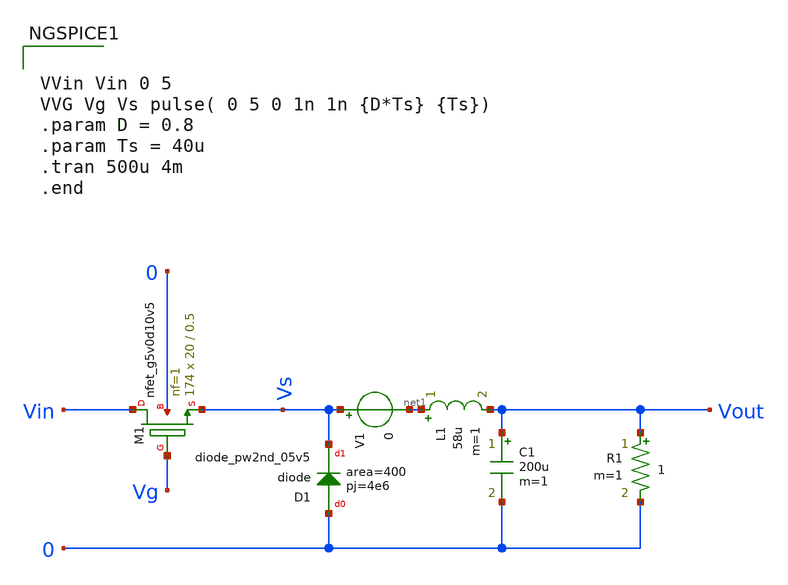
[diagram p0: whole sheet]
** sch_path: Analog_blocks/Analog_Blocks/DC_DC converter/Testbench/Buck_converter.sch
**.subckt Buck_converter
C1 Vout 0 200u m=1
L1 net1 Vout 58u m=1
R1 Vout 0 1 m=1
XM1 Vin Vg Vs 0 sky130_fd_pr__nfet_g5v0d10v5 L=0.5 W=20 nf=1 ad='int((nf+1)/2) * W/nf * 0.29' as='int((nf+2)/2) * W/nf * 0.29'
+ pd='2*int((nf+1)/2) * (W/nf + 0.29)' ps='2*int((nf+2)/2) * (W/nf + 0.29)' nrd='0.29 / W' nrs='0.29 / W'
+ sa=0 sb=0 sd=0 mult=174 m=174
V1 Vs net1 0
XD1 0 Vs sky130_fd_pr__diode_pw2nd_05v5 area=400 pj=4e6
**** begin user architecture code


VVin Vin 0 5
VVG Vg Vs pulse( 0 5 0 1n 1n {D*Ts} {Ts})
.param D = 0.8
.param Ts = 40u
.tran 500u 4m
.end




.param mc_mm_switch=0
.param mc_pr_switch=0
.include ~/mabrains/Analog_blocks/models/sky130A/libs.ref/sky130_fd_pr/spice/sky130_fd_pr__nfet_01v8__tt.corner.spice
.include ~/mabrains/Analog_blocks/models/sky130A/libs.ref/sky130_fd_pr/spice/sky130_fd_pr__nfet_01v8_lvt__tt.corner.spice
.include ~/mabrains/Analog_blocks/models/sky130A/libs.ref/sky130_fd_pr/spice/sky130_fd_pr__pfet_01v8__tt.corner.spice
.include ~/mabrains/Analog_blocks/models/sky130A/libs.ref/sky130_fd_pr/spice/sky130_fd_pr__nfet_03v3_nvt__tt.corner.spice
.include ~/mabrains/Analog_blocks/models/sky130A/libs.ref/sky130_fd_pr/spice/sky130_fd_pr__nfet_05v0_nvt__tt.corner.spice
.include ~/mabrains/Analog_blocks/models/sky130A/libs.ref/sky130_fd_pr/spice/sky130_fd_pr__esd_nfet_01v8__tt.corner.spice
.include ~/mabrains/Analog_blocks/models/sky130A/libs.ref/sky130_fd_pr/spice/sky130_fd_pr__pfet_01v8_lvt__tt.corner.spice
.include ~/mabrains/Analog_blocks/models/sky130A/libs.ref/sky130_fd_pr/spice/sky130_fd_pr__pfet_01v8_hvt__tt.corner.spice
.include ~/mabrains/Analog_blocks/models/sky130A/libs.ref/sky130_fd_pr/spice/sky130_fd_pr__esd_pfet_g5v0d10v5__tt.corner.spice
.include ~/mabrains/Analog_blocks/models/sky130A/libs.ref/sky130_fd_pr/spice/sky130_fd_pr__pfet_g5v0d10v5__tt.corner.spice
.include ~/mabrains/Analog_blocks/models/sky130A/libs.ref/sky130_fd_pr/spice/sky130_fd_pr__pfet_g5v0d16v0__tt.corner.spice
.include ~/mabrains/Analog_blocks/models/sky130A/libs.ref/sky130_fd_pr/spice/sky130_fd_pr__nfet_g5v0d10v5__tt.corner.spice
.include ~/mabrains/Analog_blocks/models/sky130A/libs.ref/sky130_fd_pr/spice/sky130_fd_pr__nfet_g5v0d16v0__tt_discrete.corner.spice
.include ~/mabrains/Analog_blocks/models/sky130A/libs.ref/sky130_fd_pr/spice/sky130_fd_pr__esd_nfet_g5v0d10v5__tt.corner.spice
.include ~/mabrains/Analog_blocks/models/sky130A/libs.tech/ngspice/corners/tt/nonfet.spice
* Mismatch parameters
.include ~/mabrains/Analog_blocks/models/sky130A/libs.ref/sky130_fd_pr/spice/sky130_fd_pr__nfet_01v8__mismatch.corner.spice
.include ~/mabrains/Analog_blocks/models/sky130A/libs.ref/sky130_fd_pr/spice/sky130_fd_pr__pfet_01v8__mismatch.corner.spice
.include ~/mabrains/Analog_blocks/models/sky130A/libs.ref/sky130_fd_pr/spice/sky130_fd_pr__nfet_01v8_lvt__mismatch.corner.spice
.include ~/mabrains/Analog_blocks/models/sky130A/libs.ref/sky130_fd_pr/spice/sky130_fd_pr__pfet_01v8_lvt__mismatch.corner.spice
.include ~/mabrains/Analog_blocks/models/sky130A/libs.ref/sky130_fd_pr/spice/sky130_fd_pr__pfet_01v8_hvt__mismatch.corner.spice
.include ~/mabrains/Analog_blocks/models/sky130A/libs.ref/sky130_fd_pr/spice/sky130_fd_pr__nfet_g5v0d10v5__mismatch.corner.spice
.include ~/mabrains/Analog_blocks/models/sky130A/libs.ref/sky130_fd_pr/spice/sky130_fd_pr__pfet_g5v0d10v5__mismatch.corner.spice
.include ~/mabrains/Analog_blocks/models/sky130A/libs.ref/sky130_fd_pr/spice/sky130_fd_pr__nfet_05v0_nvt__mismatch.corner.spice
.include ~/mabrains/Analog_blocks/models/sky130A/libs.ref/sky130_fd_pr/spice/sky130_fd_pr__nfet_03v3_nvt__mismatch.corner.spice
* Resistor/Capacitor
.include ~/mabrains/Analog_blocks/models/sky130A/libs.tech/ngspice/r+c/res_typical__cap_typical.spice
.include ~/mabrains/Analog_blocks/models/sky130A/libs.tech/ngspice/r+c/res_typical__cap_typical__lin.spice
* Special cells
.include ~/mabrains/Analog_blocks/models/sky130A/libs.tech/ngspice/corners/tt/specialized_cells.spice
* All models
.include ~/mabrains/Analog_blocks/models/sky130A/libs.tech/ngspice/all.spice
* Corner
.include ~/mabrains/Analog_blocks/models/sky130A/libs.tech/ngspice/corners/tt/rf.spice



**** end user architecture code
**.ends
.end
